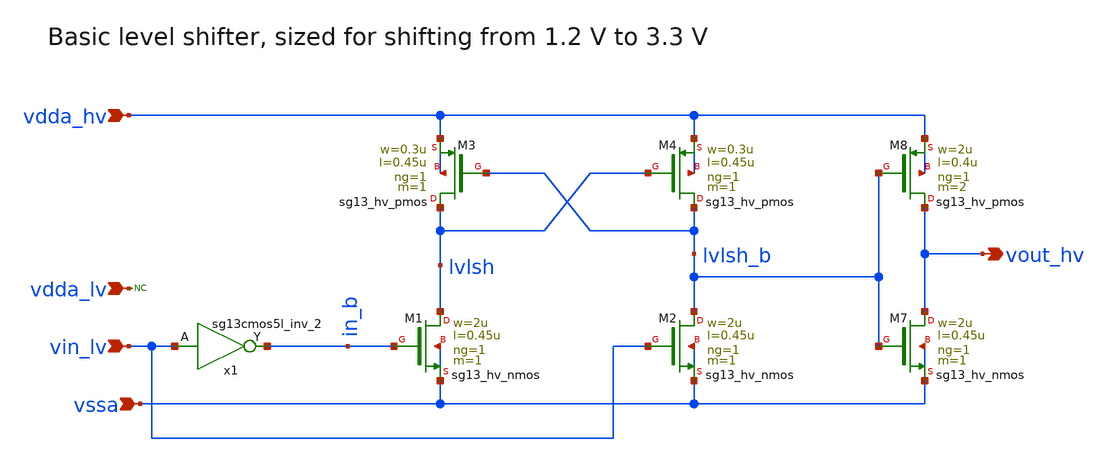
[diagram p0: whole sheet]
** sch_path: Schematics_Layout/sunrise_lvl_shft_l2h/sunrise_lvl_shft_l2h.sch
**.subckt sunrise_lvl_shft_l2h vdda_hv vdda_lv vssa vin_lv vout_hv
*.ipin vdda_hv
*.ipin vdda_lv
*.ipin vssa
*.ipin vin_lv
*.opin vout_hv
XM1 lvlsh in_b vssa vssa sg13_hv_nmos w=2u l=0.45u ng=1 m=1 mm_ok=1
XM2 lvlsh_b vin_lv vssa vssa sg13_hv_nmos w=2u l=0.45u ng=1 m=1 mm_ok=1
XM3 lvlsh lvlsh_b vdda_hv vdda_hv sg13_hv_pmos w=0.3u l=0.45u ng=1 m=1 mm_ok=1
XM4 lvlsh_b lvlsh vdda_hv vdda_hv sg13_hv_pmos w=0.3u l=0.45u ng=1 m=1 mm_ok=1
XM7 vout_hv lvlsh_b vssa vssa sg13_hv_nmos w=2u l=0.45u ng=1 m=1 mm_ok=1
XM8 vout_hv lvlsh_b vdda_hv vdda_hv sg13_hv_pmos w=2u l=0.4u ng=1 m=2 mm_ok=1
x1 in_b vin_lv vdda_lv vssa sg13cmos5l_inv_2
* noconn vdda_lv
**.ends
.end
